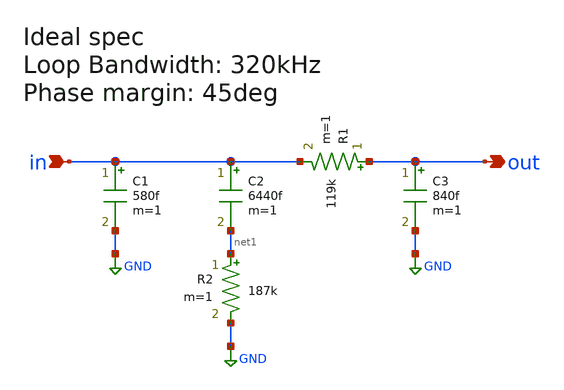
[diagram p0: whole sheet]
** sch_path: lf.sch
**.subckt lf in out
*.ipin in
*.opin out
R2 net1 GND 187k m=1
C1 in GND 580f m=1
C2 in net1 6440f m=1
R1 out in 119k m=1
C3 out GND 840f m=1
**.ends
.GLOBAL GND
.end
